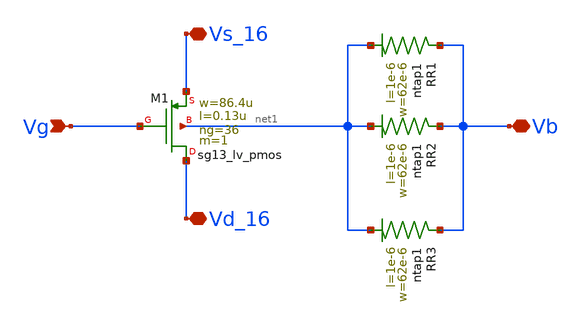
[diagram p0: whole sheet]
** sch_path: Layouts/PMOS/pmos_v2.sch
**.subckt pmos_v2 Vg Vs_16 Vd_16 Vb
*.ipin Vg
*.iopin Vs_16
*.iopin Vd_16
*.iopin Vb
XM1 Vd_16 Vg Vs_16 net1 sg13_lv_pmos w=86.4u l=0.13u ng=36 m=1 mm_ok=1
XR1 Vb net1 ntap1 R=5.213 w=62e-6 l=1e-6
XR2 Vb net1 ntap1 R=5.213 w=62e-6 l=1e-6
XR3 Vb net1 ntap1 R=5.213 w=62e-6 l=1e-6
**.ends
.end
